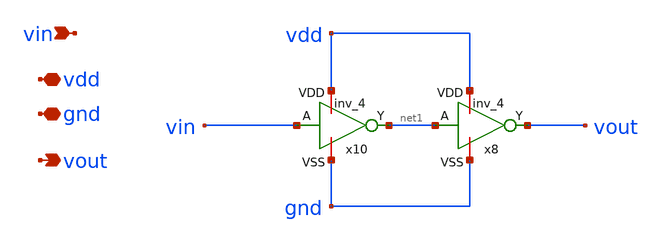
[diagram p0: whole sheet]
** sch_path: xschem/buffer.sch
**.subckt buffer vin vdd gnd vout
*.ipin vin
*.iopin vdd
*.iopin gnd
*.opin vout
x10 vdd gnd vin net1 inv_4
x8 vdd gnd net1 vout inv_4
**.ends

* expanding   symbol:  inv_4.sym # of pins=4
** sym_path: xschem/inv_4.sym
** sch_path: xschem/inv_4.sch
.subckt inv_4 VDD VSS A Y
*.opin Y
*.ipin A
*.iopin VDD
*.iopin VSS
XMN0 Y A VSS VSS sg13_lv_nmos w=2.96u l=130.00n ng=4 m=1 mm_ok=1
XMP0 Y A VDD VDD sg13_lv_pmos w=4.48u l=130.00n ng=4 m=1 mm_ok=1
.ends

.end
